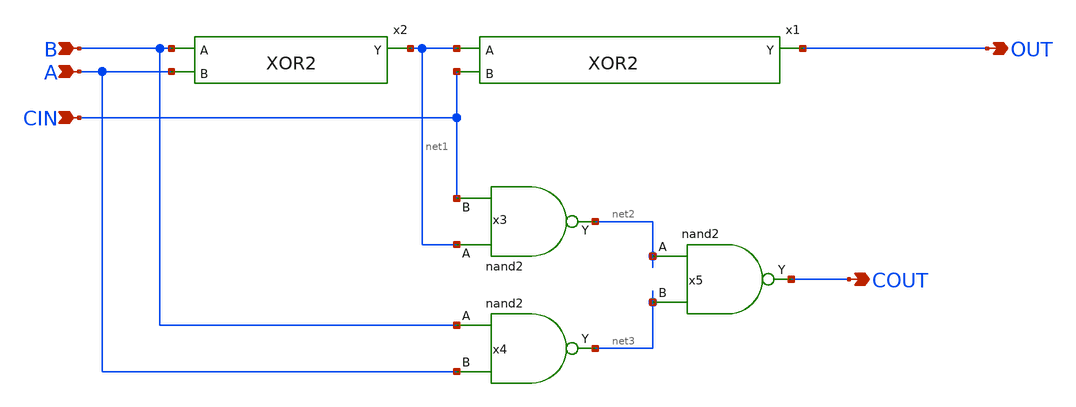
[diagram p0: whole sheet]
** sch_path: design/xschem/ADDER/full_adder.sch
**.subckt full_adder A COUT B CIN OUT
*.ipin A
*.opin COUT
*.ipin B
*.ipin CIN
*.opin OUT
x2 B A net1 VSS VDD XOR2
x1 net1 CIN OUT VSS VDD XOR2
x3 net1 CIN VSS VDD net2 nand2
x4 B A VSS VDD net3 nand2
x5 net2 net3 VSS VDD COUT nand2
**.ends
.end
